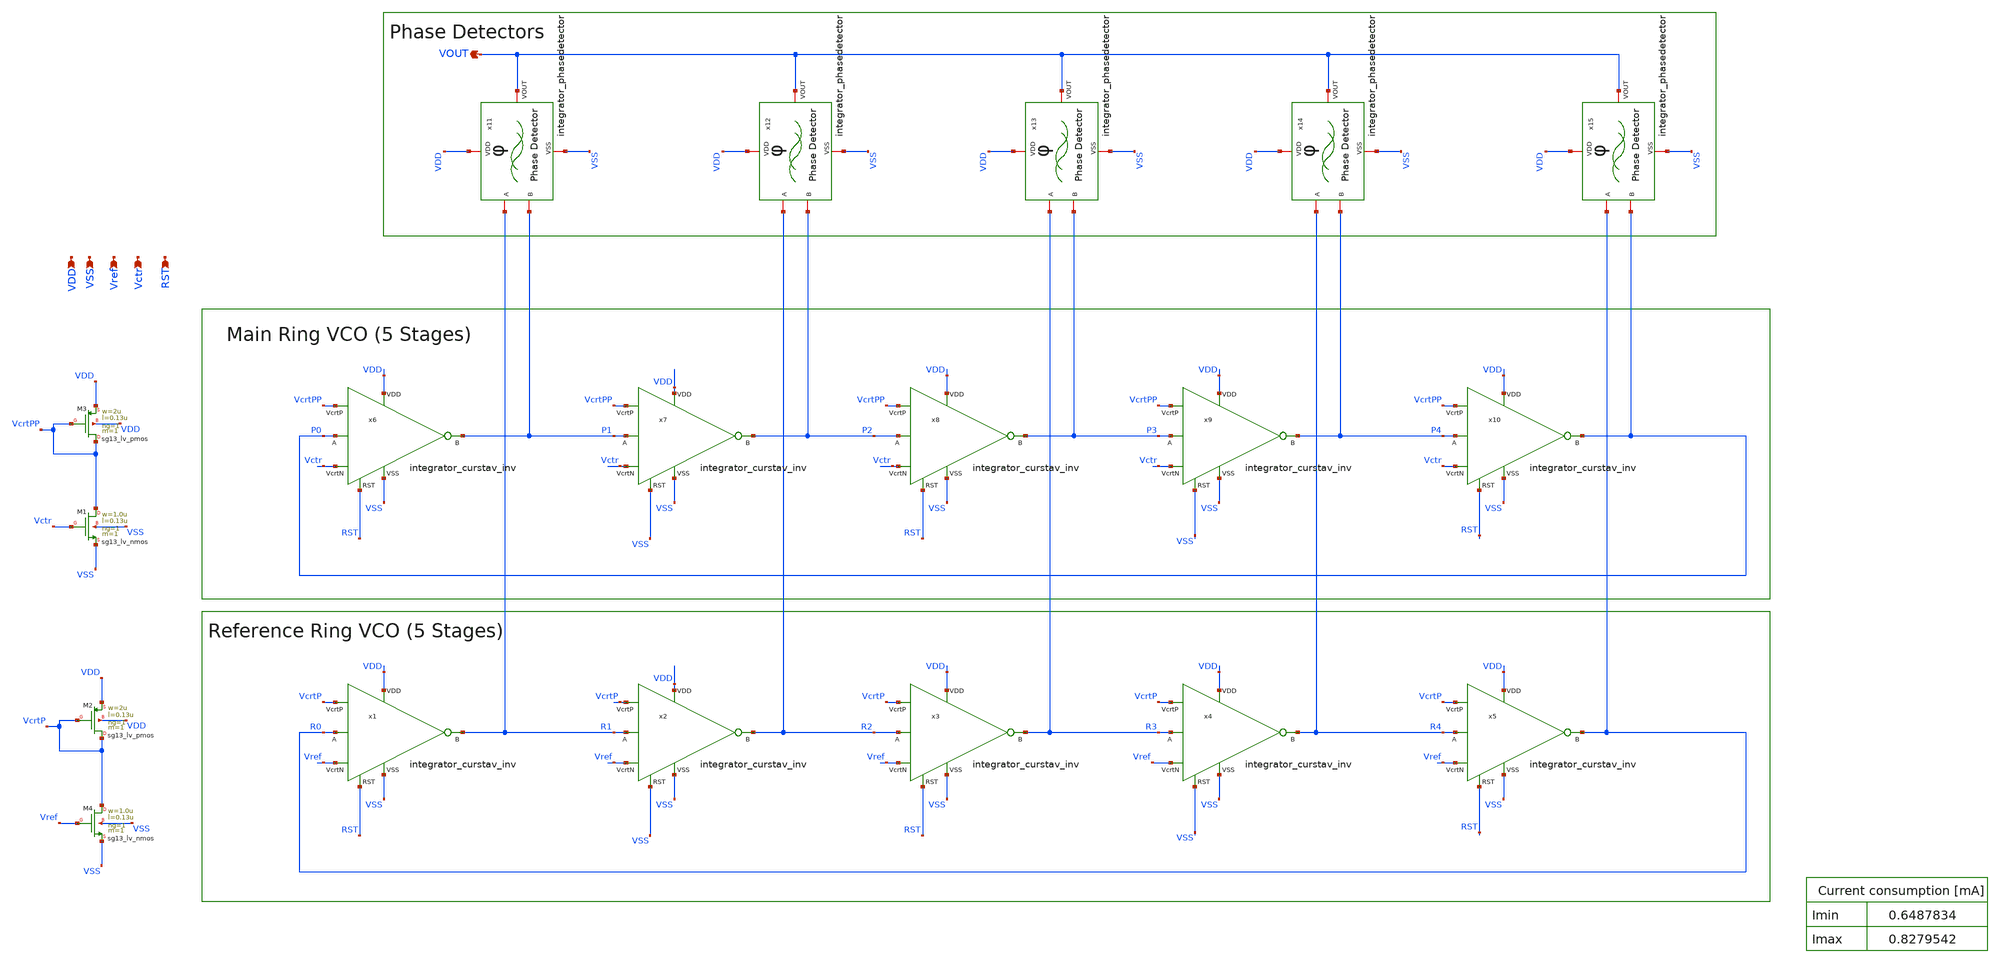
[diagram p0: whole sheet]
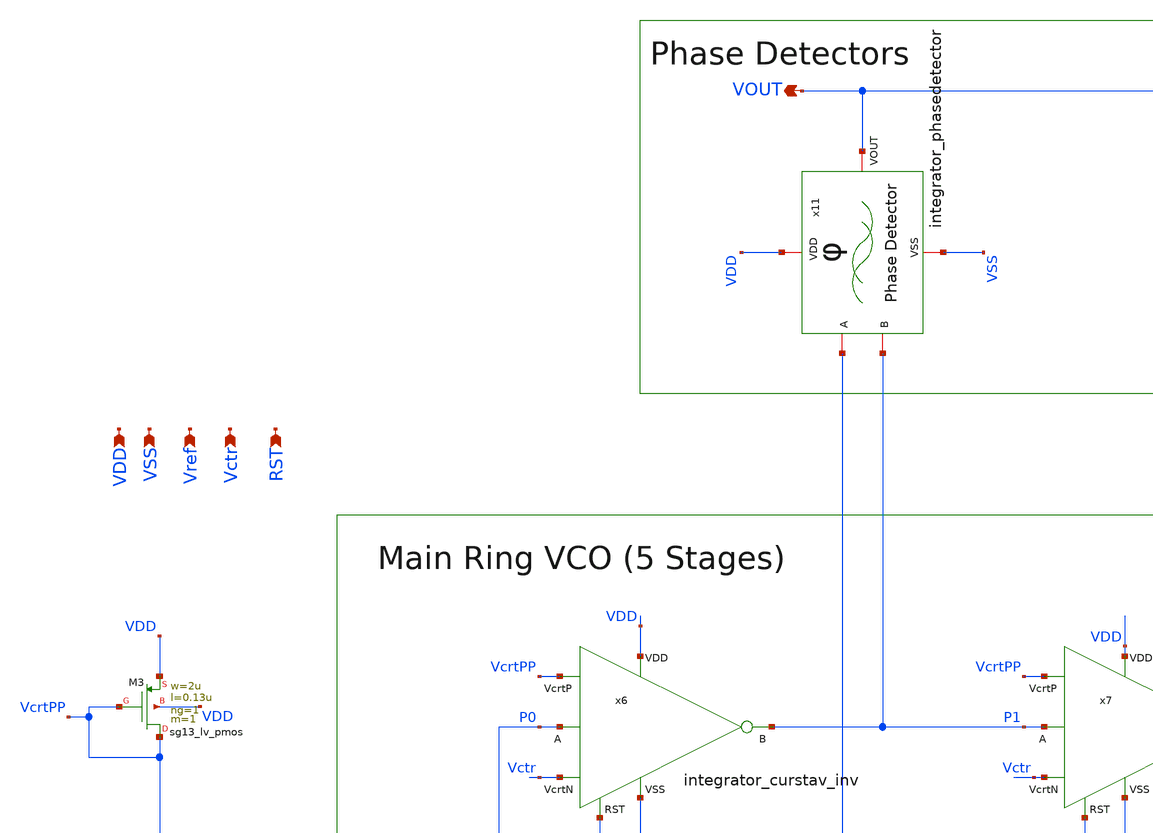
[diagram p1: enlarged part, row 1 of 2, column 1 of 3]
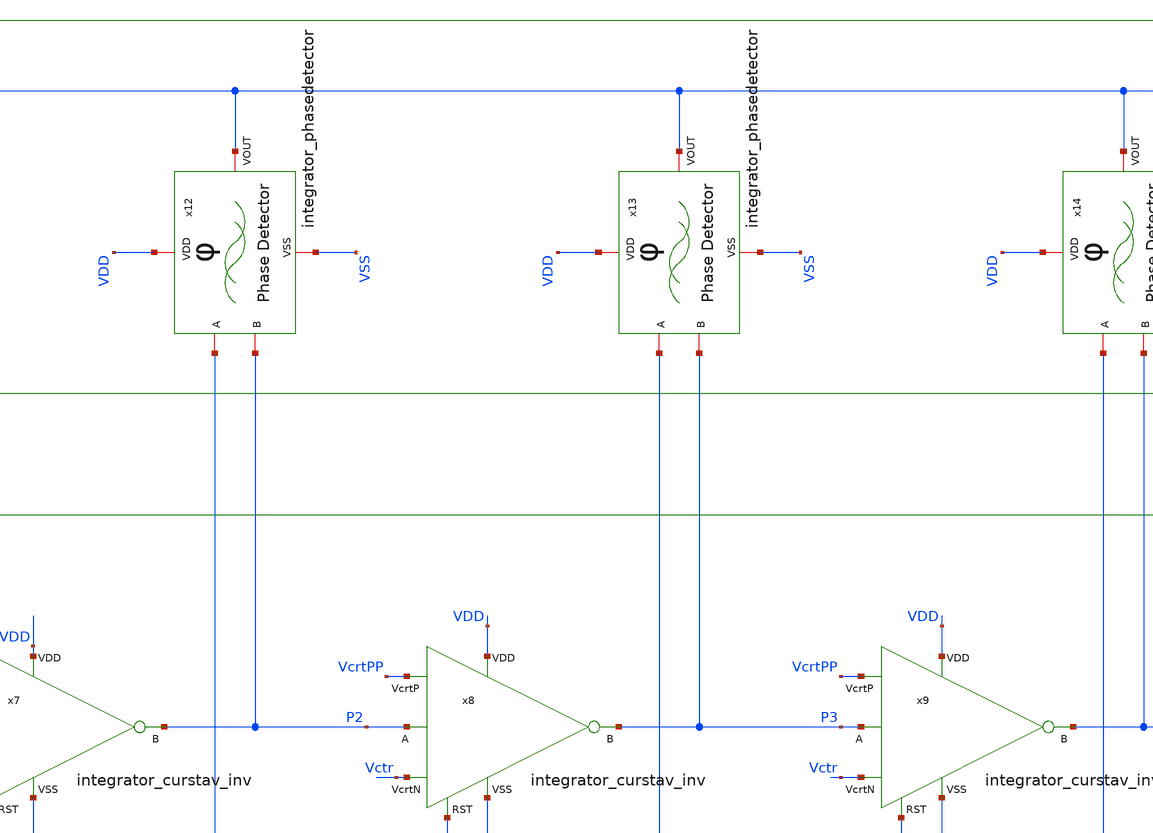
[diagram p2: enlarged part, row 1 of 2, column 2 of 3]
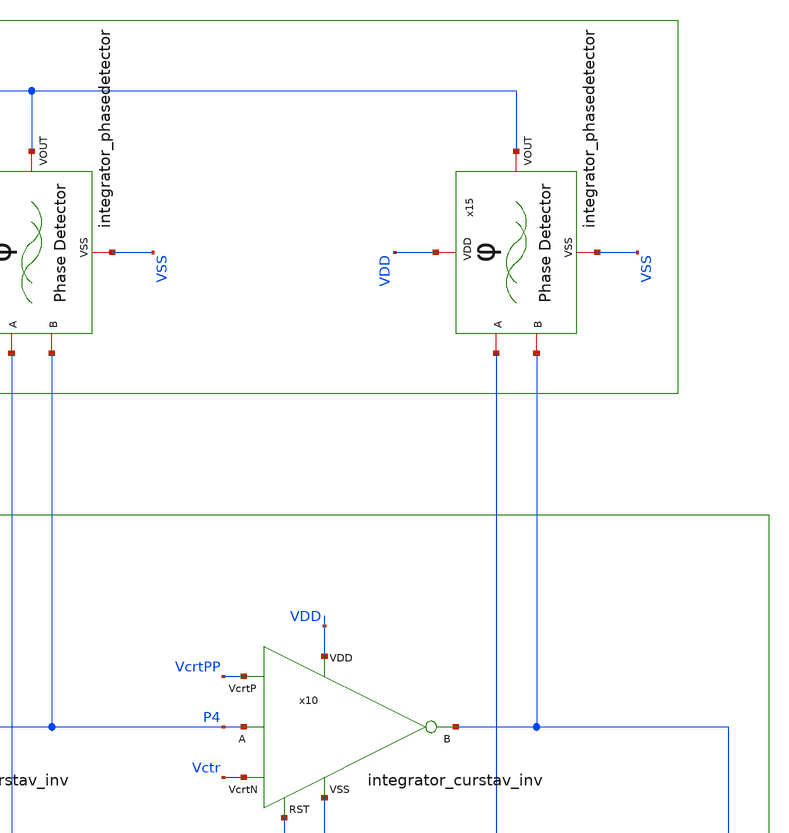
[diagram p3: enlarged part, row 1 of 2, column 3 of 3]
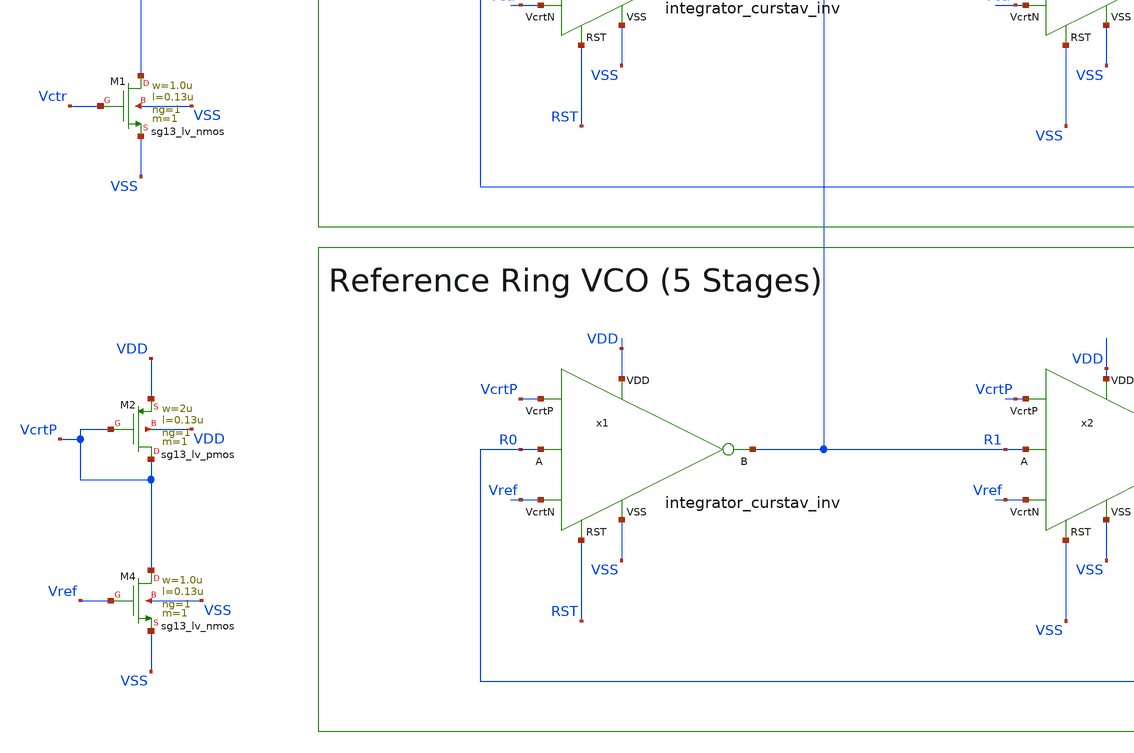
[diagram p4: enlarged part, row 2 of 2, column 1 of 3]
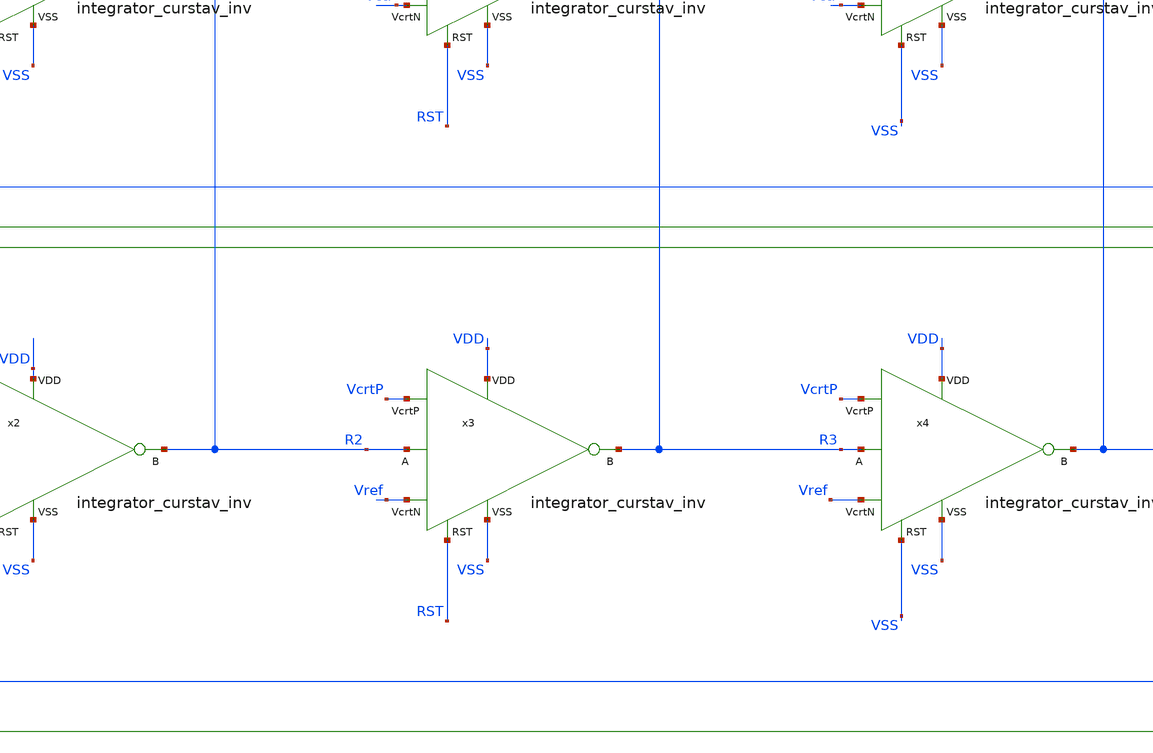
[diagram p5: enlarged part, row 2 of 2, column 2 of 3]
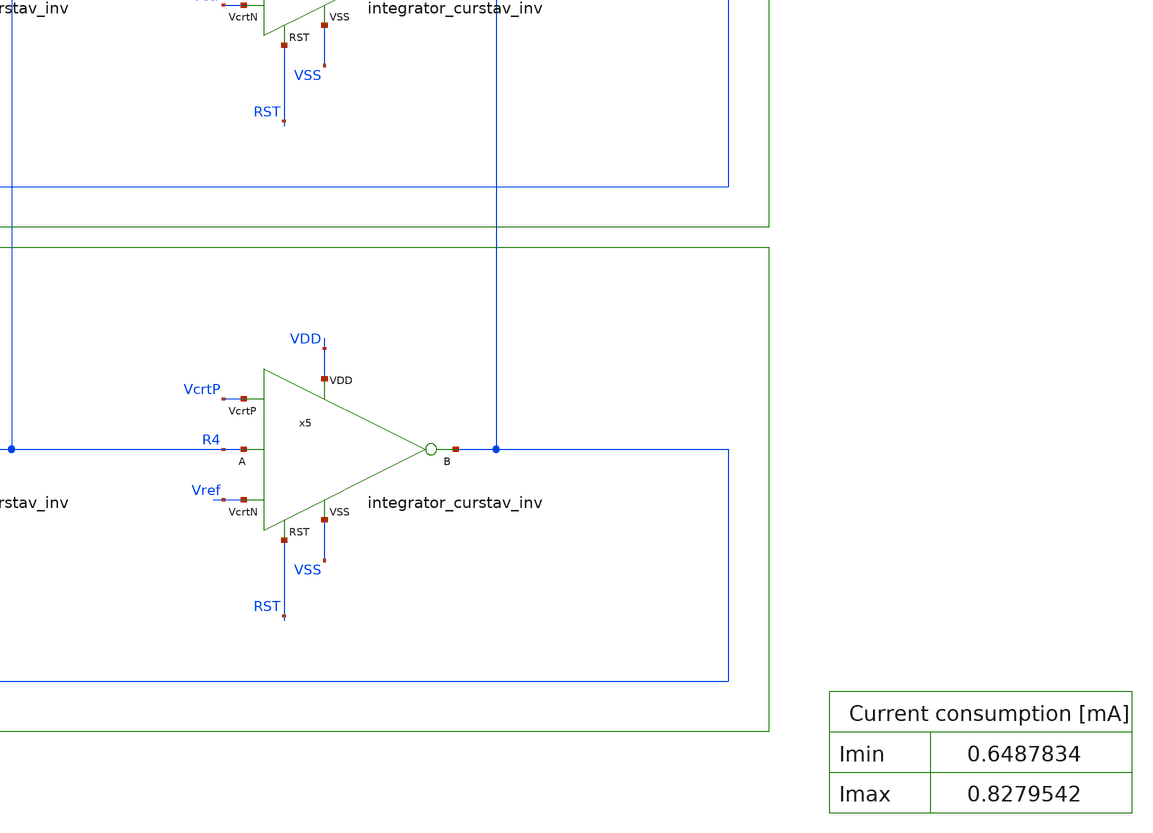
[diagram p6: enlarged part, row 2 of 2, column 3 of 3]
** sch_path: work/integrator/xschem/integrator.sch
**.subckt integrator VSS Vref Vctr VDD RST VOUT
*.ipin VSS
*.ipin Vref
*.ipin Vctr
*.ipin VDD
*.ipin RST
*.opin VOUT
x6 VDD VcrtPP P0 P1 Vctr VSS RST integrator_curstav_inv
x7 VDD VcrtPP P1 P2 Vctr VSS VSS integrator_curstav_inv
x8 VDD VcrtPP P2 P3 Vctr VSS RST integrator_curstav_inv
x9 VDD VcrtPP P3 P4 Vctr VSS VSS integrator_curstav_inv
x10 VDD VcrtPP P4 P0 Vctr VSS RST integrator_curstav_inv
x11 VDD R1 VOUT P1 VSS integrator_phasedetector
x12 VDD R2 VOUT P2 VSS integrator_phasedetector
x13 VDD R3 VOUT P3 VSS integrator_phasedetector
x14 VDD R4 VOUT P4 VSS integrator_phasedetector
x15 VDD R0 VOUT P0 VSS integrator_phasedetector
XM1 VcrtPP Vctr VSS VSS sg13_lv_nmos w=1.0u l=0.13u ng=1 m=1 mm_ok=1
XM3 VcrtPP VcrtPP VDD VDD sg13_lv_pmos w=2u l=0.13u ng=1 m=1 mm_ok=1
XM2 VcrtP VcrtP VDD VDD sg13_lv_pmos w=2u l=0.13u ng=1 m=1 mm_ok=1
XM4 VcrtP Vref VSS VSS sg13_lv_nmos w=1.0u l=0.13u ng=1 m=1 mm_ok=1
x1 VDD VcrtP R0 R1 Vref VSS RST integrator_curstav_inv
x2 VDD VcrtP R1 R2 Vref VSS VSS integrator_curstav_inv
x3 VDD VcrtP R2 R3 Vref VSS RST integrator_curstav_inv
x4 VDD VcrtP R3 R4 Vref VSS VSS integrator_curstav_inv
x5 VDD VcrtP R4 R0 Vref VSS RST integrator_curstav_inv
**.ends
.end
